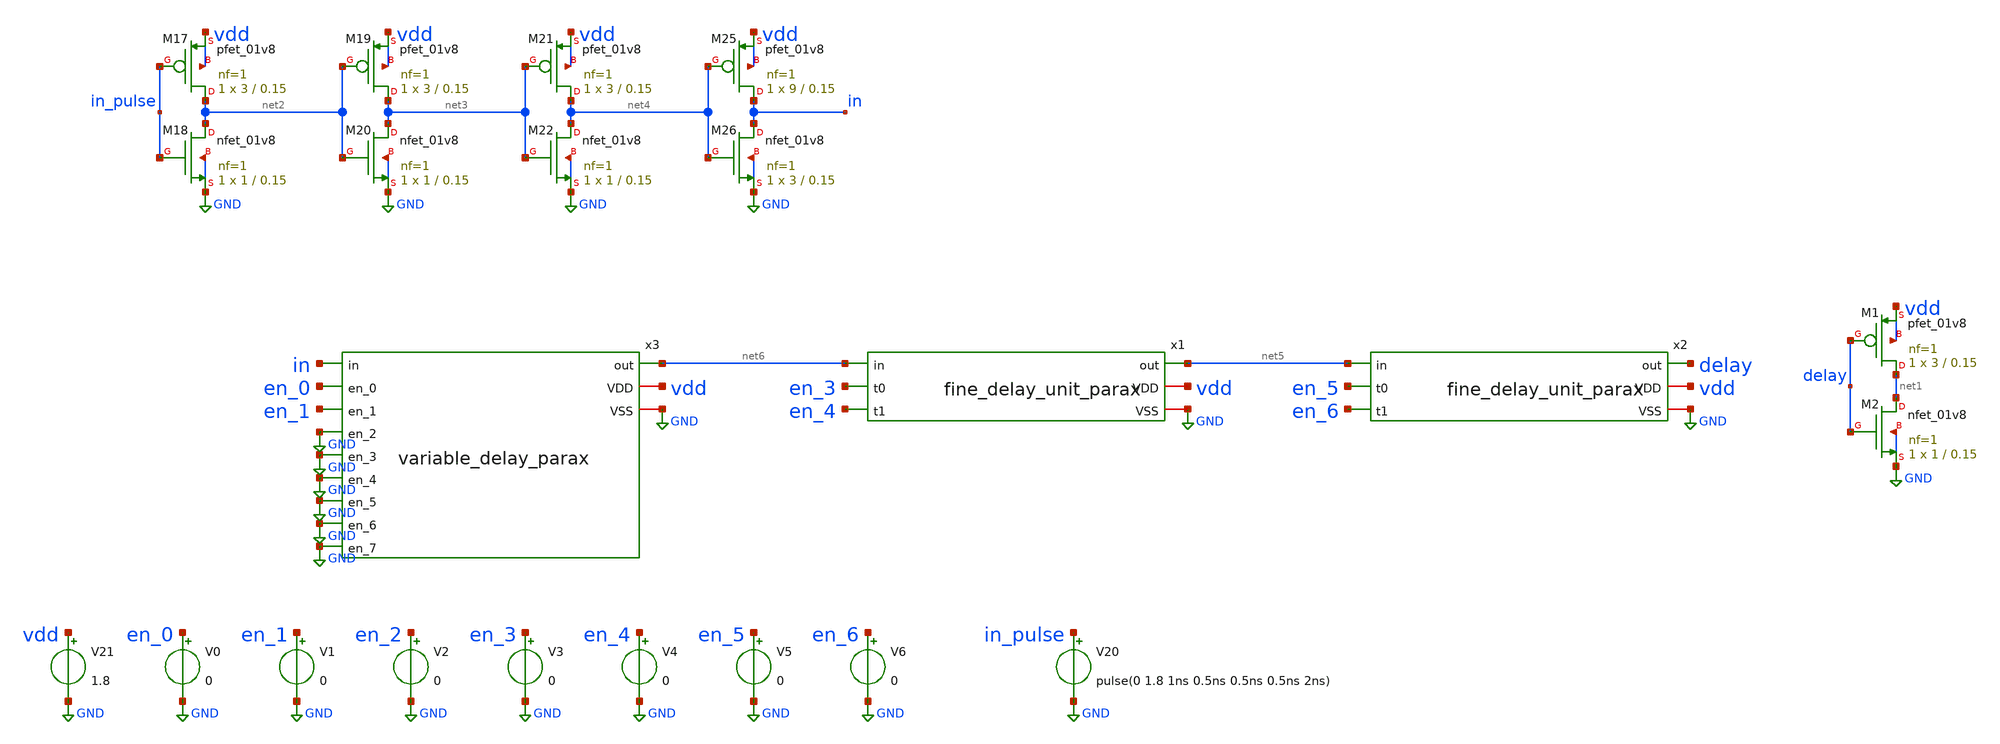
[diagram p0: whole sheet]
** sch_path: xschem/variable_delay_fine_delay_tb.sch
**.subckt variable_delay_fine_delay_tb
V21 vdd GND 1.8
V20 in_pulse GND pulse(0 1.8 1ns 0.5ns 0.5ns 0.5ns 2ns)
XM1 net1 delay vdd vdd sky130_fd_pr__pfet_01v8 L=0.15 W=3 nf=1 ad='int((nf+1)/2) * W/nf * 0.29' as='int((nf+2)/2) * W/nf * 0.29'
+ pd='2*int((nf+1)/2) * (W/nf + 0.29)' ps='2*int((nf+2)/2) * (W/nf + 0.29)' nrd='0.29 / W' nrs='0.29 / W'
+ sa=0 sb=0 sd=0 mult=1 m=1
XM2 net1 delay GND GND sky130_fd_pr__nfet_01v8 L=0.15 W=1 nf=1 ad='int((nf+1)/2) * W/nf * 0.29' as='int((nf+2)/2) * W/nf * 0.29'
+ pd='2*int((nf+1)/2) * (W/nf + 0.29)' ps='2*int((nf+2)/2) * (W/nf + 0.29)' nrd='0.29 / W' nrs='0.29 / W'
+ sa=0 sb=0 sd=0 mult=1 m=1
V0 en_0 GND 0
V1 en_1 GND 0
V2 en_2 GND 0
V3 en_3 GND 0
XM17 net2 in_pulse vdd vdd sky130_fd_pr__pfet_01v8 L=0.15 W=3 nf=1 ad='int((nf+1)/2) * W/nf * 0.29' as='int((nf+2)/2) * W/nf * 0.29'
+ pd='2*int((nf+1)/2) * (W/nf + 0.29)' ps='2*int((nf+2)/2) * (W/nf + 0.29)' nrd='0.29 / W' nrs='0.29 / W'
+ sa=0 sb=0 sd=0 mult=1 m=1
XM18 net2 in_pulse GND GND sky130_fd_pr__nfet_01v8 L=0.15 W=1 nf=1 ad='int((nf+1)/2) * W/nf * 0.29' as='int((nf+2)/2) * W/nf * 0.29'
+ pd='2*int((nf+1)/2) * (W/nf + 0.29)' ps='2*int((nf+2)/2) * (W/nf + 0.29)' nrd='0.29 / W' nrs='0.29 / W'
+ sa=0 sb=0 sd=0 mult=1 m=1
XM19 net3 net2 vdd vdd sky130_fd_pr__pfet_01v8 L=0.15 W=3 nf=1 ad='int((nf+1)/2) * W/nf * 0.29' as='int((nf+2)/2) * W/nf * 0.29'
+ pd='2*int((nf+1)/2) * (W/nf + 0.29)' ps='2*int((nf+2)/2) * (W/nf + 0.29)' nrd='0.29 / W' nrs='0.29 / W'
+ sa=0 sb=0 sd=0 mult=1 m=1
XM20 net3 net2 GND GND sky130_fd_pr__nfet_01v8 L=0.15 W=1 nf=1 ad='int((nf+1)/2) * W/nf * 0.29' as='int((nf+2)/2) * W/nf * 0.29'
+ pd='2*int((nf+1)/2) * (W/nf + 0.29)' ps='2*int((nf+2)/2) * (W/nf + 0.29)' nrd='0.29 / W' nrs='0.29 / W'
+ sa=0 sb=0 sd=0 mult=1 m=1
XM21 net4 net3 vdd vdd sky130_fd_pr__pfet_01v8 L=0.15 W=3 nf=1 ad='int((nf+1)/2) * W/nf * 0.29' as='int((nf+2)/2) * W/nf * 0.29'
+ pd='2*int((nf+1)/2) * (W/nf + 0.29)' ps='2*int((nf+2)/2) * (W/nf + 0.29)' nrd='0.29 / W' nrs='0.29 / W'
+ sa=0 sb=0 sd=0 mult=1 m=1
XM22 net4 net3 GND GND sky130_fd_pr__nfet_01v8 L=0.15 W=1 nf=1 ad='int((nf+1)/2) * W/nf * 0.29' as='int((nf+2)/2) * W/nf * 0.29'
+ pd='2*int((nf+1)/2) * (W/nf + 0.29)' ps='2*int((nf+2)/2) * (W/nf + 0.29)' nrd='0.29 / W' nrs='0.29 / W'
+ sa=0 sb=0 sd=0 mult=1 m=1
XM25 in net4 vdd vdd sky130_fd_pr__pfet_01v8 L=0.15 W=9 nf=1 ad='int((nf+1)/2) * W/nf * 0.29' as='int((nf+2)/2) * W/nf * 0.29'
+ pd='2*int((nf+1)/2) * (W/nf + 0.29)' ps='2*int((nf+2)/2) * (W/nf + 0.29)' nrd='0.29 / W' nrs='0.29 / W'
+ sa=0 sb=0 sd=0 mult=1 m=1
XM26 in net4 GND GND sky130_fd_pr__nfet_01v8 L=0.15 W=3 nf=1 ad='int((nf+1)/2) * W/nf * 0.29' as='int((nf+2)/2) * W/nf * 0.29'
+ pd='2*int((nf+1)/2) * (W/nf + 0.29)' ps='2*int((nf+2)/2) * (W/nf + 0.29)' nrd='0.29 / W' nrs='0.29 / W'
+ sa=0 sb=0 sd=0 mult=1 m=1
x1 net6 en_3 en_4 net5 vdd GND fine_delay_unit_parax
x2 net5 en_5 en_6 delay vdd GND fine_delay_unit_parax
V4 en_4 GND 0
x3 in en_0 en_1 GND GND GND GND GND GND net6 vdd GND variable_delay_parax
V5 en_5 GND 0
V6 en_6 GND 0
**** begin user architecture code

** opencircuitdesign pdks install
.lib $::SKYWATER_MODELS/sky130.lib.spice tt





.control
alter V0 0
alter V1 1.8
alter V2 0
alter V3 0
alter V4 0
alter V5 0
alter V6 0

tran 0.0001n 5n
save v(in) v(delay)
set wr_vecnames
wrdata variable_delay_fine_delay_tb_1 v(in) v(delay)

alter V0 1.8
alter V1 0

foreach i 2 3 4 5 6
alter V$i 1.8

* Run transient analysis
tran 0.0001n 5n

* Save results for this step
save v(in) v(delay)
set wr_vecnames
wrdata variable_delay_fine_delay_tb_$i v(in) v(delay)

end
.endc


**** end user architecture code
**.ends

* expanding   symbol:  fine_delay_unit_parax.sym # of pins=6
** sym_path: xschem/fine_delay.sym
.include [file normalize ../mag/fine_delay_unit.sim.spice]

* expanding   symbol:  variable_delay_parax.sym # of pins=12
** sym_path: xschem/variable_delay.sym
.include [file normalize ../mag/variable_delay.sim.spice]
.GLOBAL GND
.end
